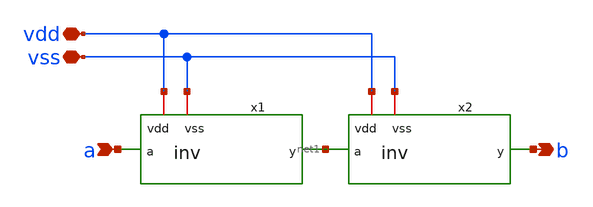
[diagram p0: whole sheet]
** sch_path: member_project/ice458/dynamic_comparator/xschem/inv2.sch
**.subckt inv2 a b vdd vss
*.ipin a
*.opin b
*.iopin vdd
*.iopin vss
x1 vdd a net1 vss inv
x2 vdd net1 b vss inv
**.ends

* expanding   symbol:  inv.sym # of pins=4
** sym_path: member_project/ice458/dynamic_comparator/xschem/inv.sym
** sch_path: member_project/ice458/dynamic_comparator/xschem/inv.sch
.subckt inv vdd a y vss
*.iopin vdd
*.iopin vss
*.ipin a
*.opin y
XM1 y a vss vss nfet_03v3 L=0.28u W=0.42u nf=1 ad='int((nf+1)/2) * W/nf * 0.18u' as='int((nf+2)/2) * W/nf * 0.18u'
+ pd='2*int((nf+1)/2) * (W/nf + 0.18u)' ps='2*int((nf+2)/2) * (W/nf + 0.18u)' nrd='0.18u / W' nrs='0.18u / W'
+ sa=0 sb=0 sd=0 m=1
XM2 y a vdd vdd pfet_03v3 L=0.28u W=1u nf=1 ad='int((nf+1)/2) * W/nf * 0.18u' as='int((nf+2)/2) * W/nf * 0.18u'
+ pd='2*int((nf+1)/2) * (W/nf + 0.18u)' ps='2*int((nf+2)/2) * (W/nf + 0.18u)' nrd='0.18u / W' nrs='0.18u / W'
+ sa=0 sb=0 sd=0 m=1
.ends

.end
